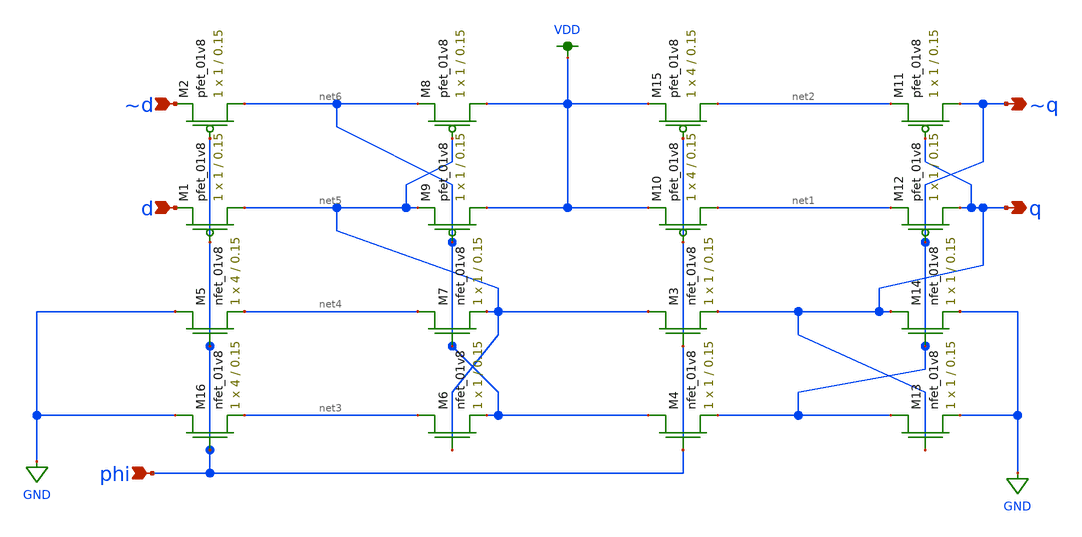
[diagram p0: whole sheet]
** sch_path: mini_proj_2/schematic/dff_4_wide.sch
**.subckt dff_4_wide phi d ~d ~q q
*.ipin phi
*.ipin d
*.ipin ~d
*.opin ~q
*.opin q
XM4 net6 phi ~q GND sky130_fd_pr__nfet_01v8 L=0.15 W=1 nf=1 ad='int((nf+1)/2) * W/nf * 0.29' as='int((nf+2)/2) * W/nf * 0.29'
+ pd='2*int((nf+1)/2) * (W/nf + 0.29)' ps='2*int((nf+2)/2) * (W/nf + 0.29)' nrd='0.29 / W' nrs='0.29 / W'
+ sa=0 sb=0 sd=0 mult=1 m=1
XM3 net5 phi q GND sky130_fd_pr__nfet_01v8 L=0.15 W=1 nf=1 ad='int((nf+1)/2) * W/nf * 0.29' as='int((nf+2)/2) * W/nf * 0.29'
+ pd='2*int((nf+1)/2) * (W/nf + 0.29)' ps='2*int((nf+2)/2) * (W/nf + 0.29)' nrd='0.29 / W' nrs='0.29 / W'
+ sa=0 sb=0 sd=0 mult=1 m=1
XM1 net5 phi d VDD sky130_fd_pr__pfet_01v8 L=0.15 W=1 nf=1 ad='int((nf+1)/2) * W/nf * 0.29' as='int((nf+2)/2) * W/nf * 0.29'
+ pd='2*int((nf+1)/2) * (W/nf + 0.29)' ps='2*int((nf+2)/2) * (W/nf + 0.29)' nrd='0.29 / W' nrs='0.29 / W'
+ sa=0 sb=0 sd=0 mult=1 m=1
XM2 net6 phi ~d VDD sky130_fd_pr__pfet_01v8 L=0.15 W=1 nf=1 ad='int((nf+1)/2) * W/nf * 0.29' as='int((nf+2)/2) * W/nf * 0.29'
+ pd='2*int((nf+1)/2) * (W/nf + 0.29)' ps='2*int((nf+2)/2) * (W/nf + 0.29)' nrd='0.29 / W' nrs='0.29 / W'
+ sa=0 sb=0 sd=0 mult=1 m=1
XM10 net1 phi VDD VDD sky130_fd_pr__pfet_01v8 L=0.15 W=4 nf=1 ad='int((nf+1)/2) * W/nf * 0.29' as='int((nf+2)/2) * W/nf * 0.29'
+ pd='2*int((nf+1)/2) * (W/nf + 0.29)' ps='2*int((nf+2)/2) * (W/nf + 0.29)' nrd='0.29 / W' nrs='0.29 / W'
+ sa=0 sb=0 sd=0 mult=1 m=1
XM13 ~q q GND GND sky130_fd_pr__nfet_01v8 L=0.15 W=1 nf=1 ad='int((nf+1)/2) * W/nf * 0.29' as='int((nf+2)/2) * W/nf * 0.29'
+ pd='2*int((nf+1)/2) * (W/nf + 0.29)' ps='2*int((nf+2)/2) * (W/nf + 0.29)' nrd='0.29 / W' nrs='0.29 / W'
+ sa=0 sb=0 sd=0 mult=1 m=1
XM14 q ~q GND GND sky130_fd_pr__nfet_01v8 L=0.15 W=1 nf=1 ad='int((nf+1)/2) * W/nf * 0.29' as='int((nf+2)/2) * W/nf * 0.29'
+ pd='2*int((nf+1)/2) * (W/nf + 0.29)' ps='2*int((nf+2)/2) * (W/nf + 0.29)' nrd='0.29 / W' nrs='0.29 / W'
+ sa=0 sb=0 sd=0 mult=1 m=1
XM6 net3 net5 net6 GND sky130_fd_pr__nfet_01v8 L=0.15 W=1 nf=1 ad='int((nf+1)/2) * W/nf * 0.29' as='int((nf+2)/2) * W/nf * 0.29'
+ pd='2*int((nf+1)/2) * (W/nf + 0.29)' ps='2*int((nf+2)/2) * (W/nf + 0.29)' nrd='0.29 / W' nrs='0.29 / W'
+ sa=0 sb=0 sd=0 mult=1 m=1
XM7 net4 net6 net5 GND sky130_fd_pr__nfet_01v8 L=0.15 W=1 nf=1 ad='int((nf+1)/2) * W/nf * 0.29' as='int((nf+2)/2) * W/nf * 0.29'
+ pd='2*int((nf+1)/2) * (W/nf + 0.29)' ps='2*int((nf+2)/2) * (W/nf + 0.29)' nrd='0.29 / W' nrs='0.29 / W'
+ sa=0 sb=0 sd=0 mult=1 m=1
XM5 GND phi net4 GND sky130_fd_pr__nfet_01v8 L=0.15 W=4 nf=1 ad='int((nf+1)/2) * W/nf * 0.29' as='int((nf+2)/2) * W/nf * 0.29'
+ pd='2*int((nf+1)/2) * (W/nf + 0.29)' ps='2*int((nf+2)/2) * (W/nf + 0.29)' nrd='0.29 / W' nrs='0.29 / W'
+ sa=0 sb=0 sd=0 mult=1 m=1
XM8 VDD net5 net6 VDD sky130_fd_pr__pfet_01v8 L=0.15 W=1 nf=1 ad='int((nf+1)/2) * W/nf * 0.29' as='int((nf+2)/2) * W/nf * 0.29'
+ pd='2*int((nf+1)/2) * (W/nf + 0.29)' ps='2*int((nf+2)/2) * (W/nf + 0.29)' nrd='0.29 / W' nrs='0.29 / W'
+ sa=0 sb=0 sd=0 mult=1 m=1
XM9 VDD net6 net5 VDD sky130_fd_pr__pfet_01v8 L=0.15 W=1 nf=1 ad='int((nf+1)/2) * W/nf * 0.29' as='int((nf+2)/2) * W/nf * 0.29'
+ pd='2*int((nf+1)/2) * (W/nf + 0.29)' ps='2*int((nf+2)/2) * (W/nf + 0.29)' nrd='0.29 / W' nrs='0.29 / W'
+ sa=0 sb=0 sd=0 mult=1 m=1
XM12 q ~q net1 VDD sky130_fd_pr__pfet_01v8 L=0.15 W=1 nf=1 ad='int((nf+1)/2) * W/nf * 0.29' as='int((nf+2)/2) * W/nf * 0.29'
+ pd='2*int((nf+1)/2) * (W/nf + 0.29)' ps='2*int((nf+2)/2) * (W/nf + 0.29)' nrd='0.29 / W' nrs='0.29 / W'
+ sa=0 sb=0 sd=0 mult=1 m=1
XM11 ~q q net2 VDD sky130_fd_pr__pfet_01v8 L=0.15 W=1 nf=1 ad='int((nf+1)/2) * W/nf * 0.29' as='int((nf+2)/2) * W/nf * 0.29'
+ pd='2*int((nf+1)/2) * (W/nf + 0.29)' ps='2*int((nf+2)/2) * (W/nf + 0.29)' nrd='0.29 / W' nrs='0.29 / W'
+ sa=0 sb=0 sd=0 mult=1 m=1
XM16 GND phi net3 GND sky130_fd_pr__nfet_01v8 L=0.15 W=4 nf=1 ad='int((nf+1)/2) * W/nf * 0.29' as='int((nf+2)/2) * W/nf * 0.29'
+ pd='2*int((nf+1)/2) * (W/nf + 0.29)' ps='2*int((nf+2)/2) * (W/nf + 0.29)' nrd='0.29 / W' nrs='0.29 / W'
+ sa=0 sb=0 sd=0 mult=1 m=1
XM15 net2 phi VDD VDD sky130_fd_pr__pfet_01v8 L=0.15 W=4 nf=1 ad='int((nf+1)/2) * W/nf * 0.29' as='int((nf+2)/2) * W/nf * 0.29'
+ pd='2*int((nf+1)/2) * (W/nf + 0.29)' ps='2*int((nf+2)/2) * (W/nf + 0.29)' nrd='0.29 / W' nrs='0.29 / W'
+ sa=0 sb=0 sd=0 mult=1 m=1
**.ends
.GLOBAL VDD
.GLOBAL GND
.end
